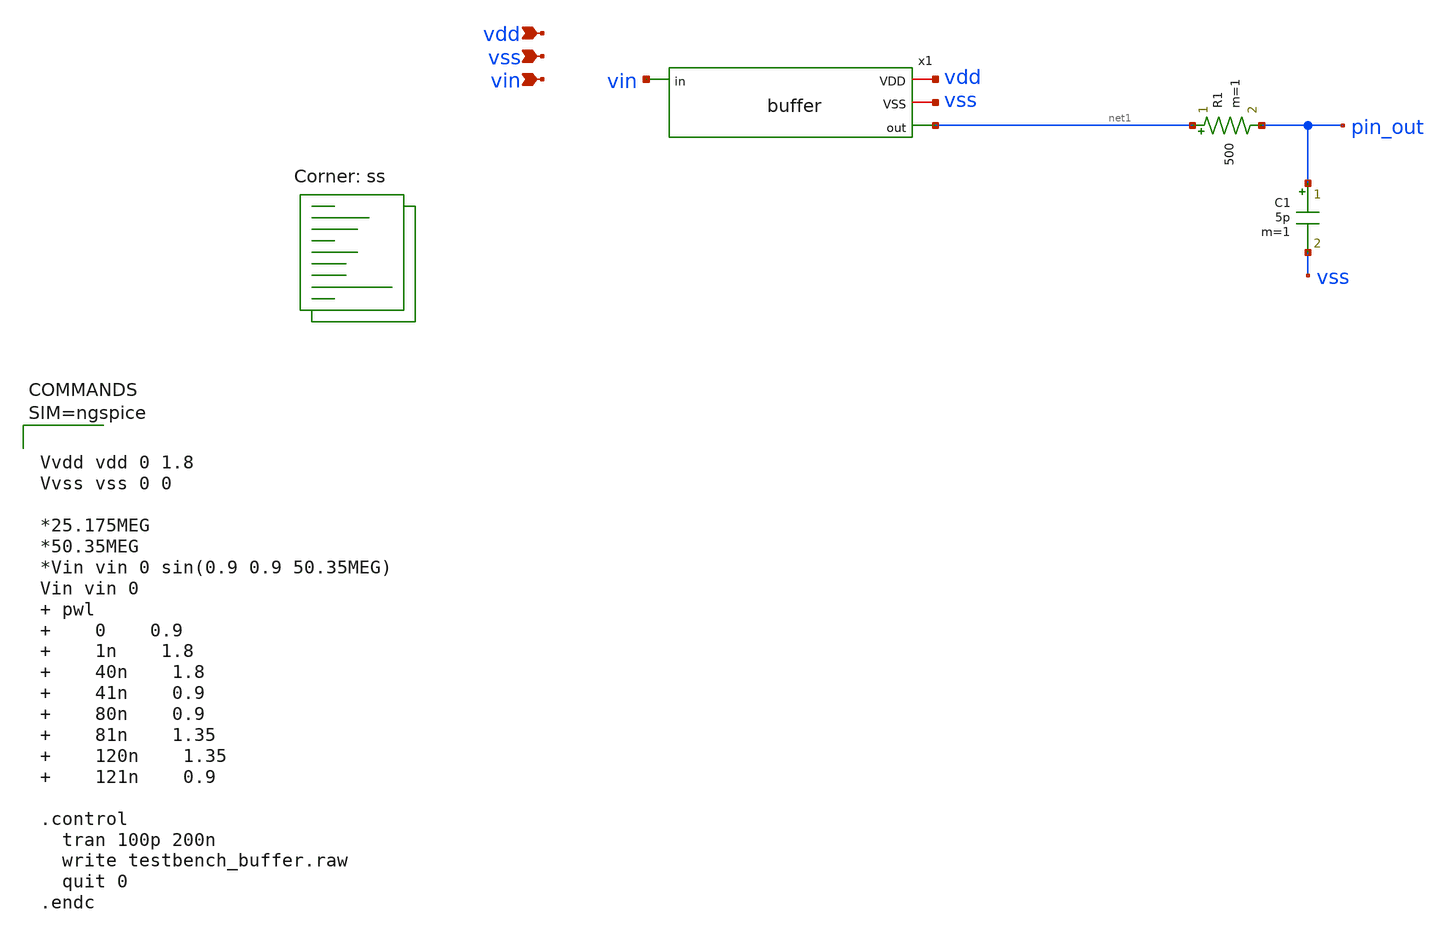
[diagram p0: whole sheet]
** sch_path: xschem/testbench_buffer.sch
**.subckt testbench_buffer vdd vss vin
*.ipin vdd
*.ipin vss
*.ipin vin
R1 net1 pin_out 500 m=1
C1 pin_out vss 5p m=1
x1 vdd vss net1 vin buffer
**** begin user architecture code



Vvdd vdd 0 1.8
Vvss vss 0 0

*25.175MEG
*50.35MEG
*Vin vin 0 sin(0.9 0.9 50.35MEG)
Vin vin 0   pwl  	0	0.9 	1n	1.8 	40n	1.8 	41n	0.9 	80n	0.9 	81n	1.35 	120n	1.35 	121n	0.9

.control
  tran 100p 200n
  write testbench_buffer.raw
  quit 0
.endc



.lib $::SKYWATER_MODELS/sky130.lib.spice ss
**** end user architecture code
**.ends

* expanding   symbol:  buffer.sym # of pins=4
** sym_path: xschem/buffer.sym
** sch_path: xschem/buffer.sch
.subckt buffer VDD VSS out in
*.iopin VSS
*.iopin VDD
*.ipin in
*.opin out
XM3 VDD in out VSS sky130_fd_pr__nfet_01v8_lvt L=0.15 W=7 nf=1 ad='int((nf+1)/2) * W/nf * 0.29' as='int((nf+2)/2) * W/nf * 0.29'
+ pd='2*int((nf+1)/2) * (W/nf + 0.29)' ps='2*int((nf+2)/2) * (W/nf + 0.29)' nrd='0.29 / W' nrs='0.29 / W'
+ sa=0 sb=0 sd=0 mult=1 m=1
XM1 out net1 VSS VSS sky130_fd_pr__nfet_01v8_lvt L=0.15 W=7 nf=1 ad='int((nf+1)/2) * W/nf * 0.29' as='int((nf+2)/2) * W/nf * 0.29'
+ pd='2*int((nf+1)/2) * (W/nf + 0.29)' ps='2*int((nf+2)/2) * (W/nf + 0.29)' nrd='0.29 / W' nrs='0.29 / W'
+ sa=0 sb=0 sd=0 mult=1 m=1
XR5 VSS net1 VSS sky130_fd_pr__res_high_po_0p35 L=40 mult=1 m=1
XR6 net1 VDD VSS sky130_fd_pr__res_high_po_0p35 L=20 mult=1 m=1
.ends

.end
